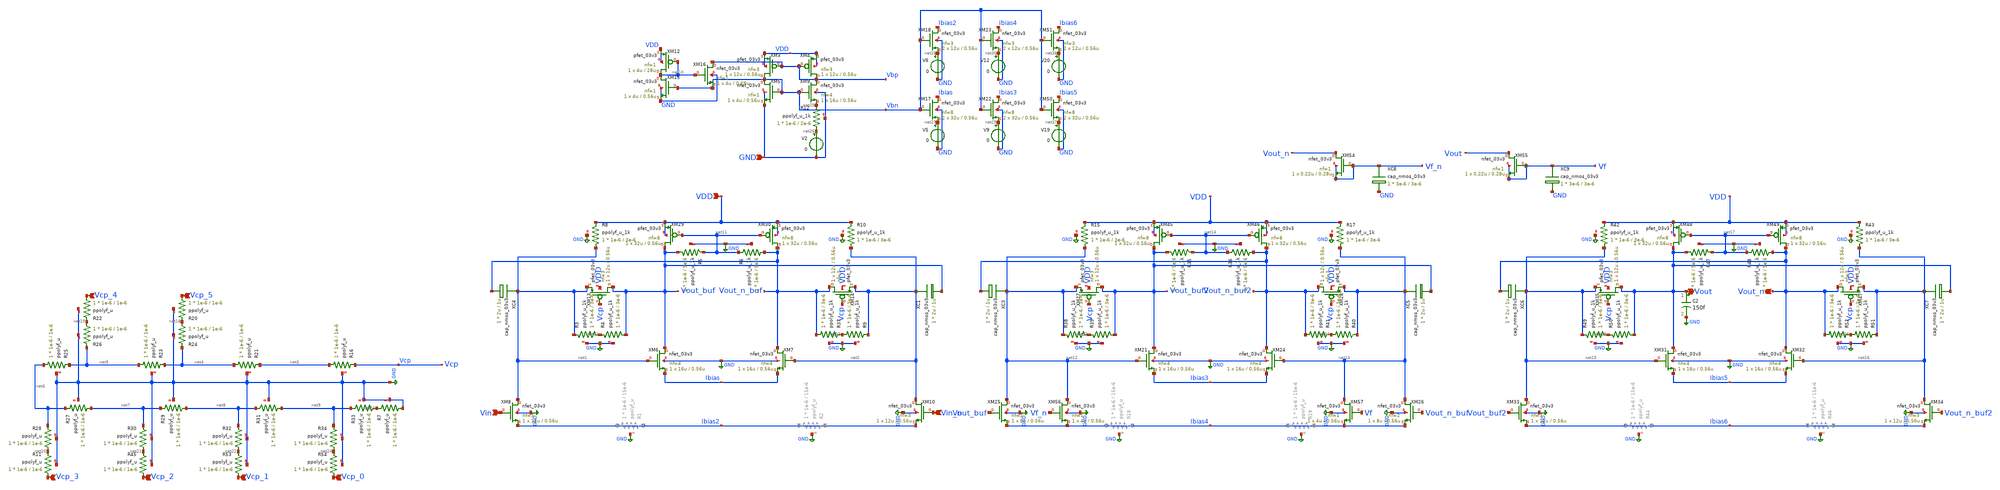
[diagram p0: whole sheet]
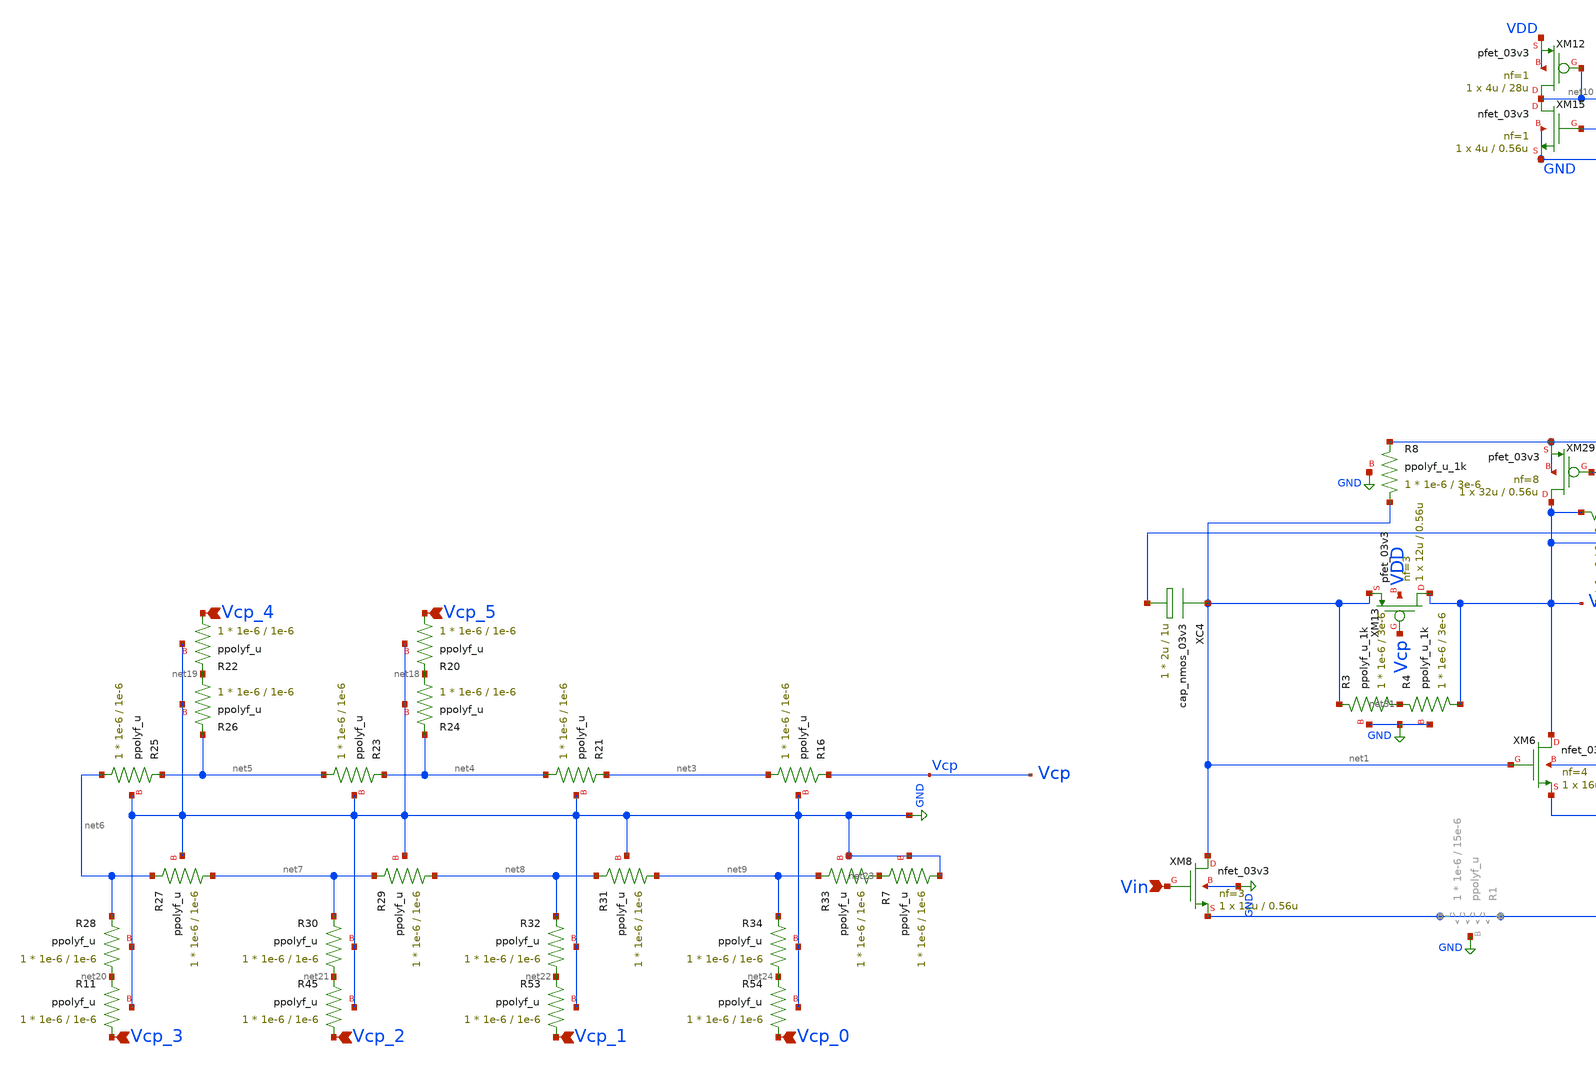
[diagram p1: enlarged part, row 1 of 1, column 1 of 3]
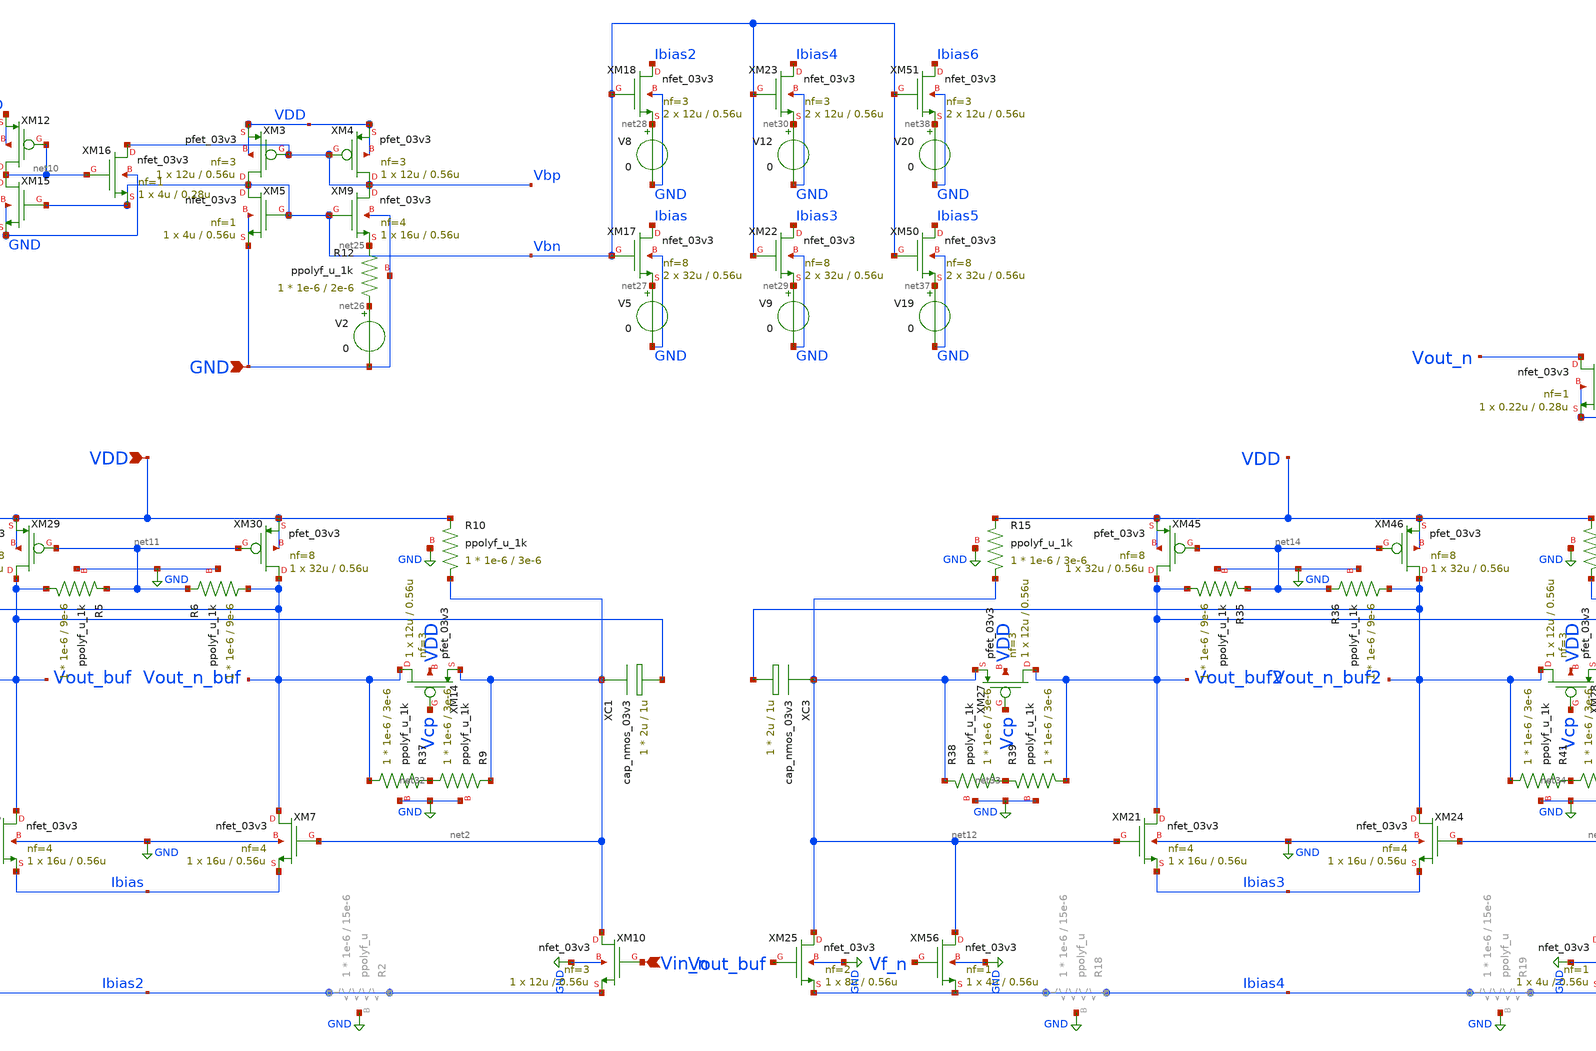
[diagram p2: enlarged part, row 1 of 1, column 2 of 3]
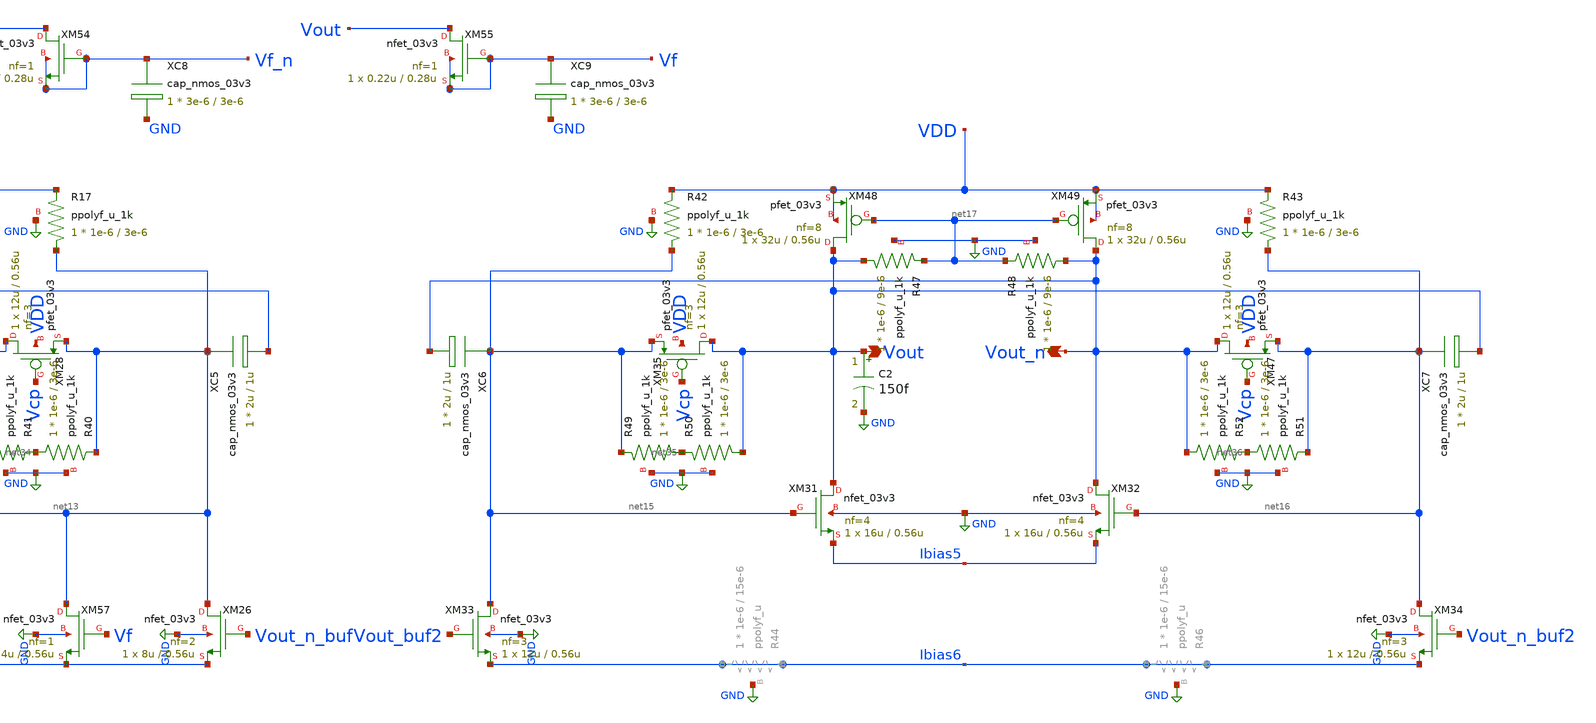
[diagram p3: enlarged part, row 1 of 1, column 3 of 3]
** sch_path: blocks/adc/vga/vga.sch
**.subckt vga Vcp_0 Vcp_1 Vcp_2 Vcp_3 Vcp_4 Vcp_5 VDD Vin Vin_n Vout GND Vout_n
*.ipin Vcp_0
*.ipin Vcp_1
*.ipin Vcp_2
*.ipin Vcp_3
*.ipin Vcp_4
*.ipin Vcp_5
*.ipin VDD
*.ipin Vin
*.ipin Vin_n
*.opin Vout
*.ipin GND
*.opin Vout_n
XM6 Vout_buf net1 Ibias GND nfet_03v3 L=0.56u W=16u nf=4 ad='int((nf+1)/2) * W/nf * 0.18u' as='int((nf+2)/2) * W/nf * 0.18u'
+ pd='2*int((nf+1)/2) * (W/nf + 0.18u)' ps='2*int((nf+2)/2) * (W/nf + 0.18u)' nrd='0.18u / W' nrs='0.18u / W'
+ sa=0 sb=0 sd=0 m=1
XM7 Vout_n_buf net2 Ibias GND nfet_03v3 L=0.56u W=16u nf=4 ad='int((nf+1)/2) * W/nf * 0.18u' as='int((nf+2)/2) * W/nf * 0.18u'
+ pd='2*int((nf+1)/2) * (W/nf + 0.18u)' ps='2*int((nf+2)/2) * (W/nf + 0.18u)' nrd='0.18u / W' nrs='0.18u / W'
+ sa=0 sb=0 sd=0 m=1
XM8 net1 Vin Ibias2 GND nfet_03v3 L=0.56u W=12u nf=3 ad='int((nf+1)/2) * W/nf * 0.18u' as='int((nf+2)/2) * W/nf * 0.18u'
+ pd='2*int((nf+1)/2) * (W/nf + 0.18u)' ps='2*int((nf+2)/2) * (W/nf + 0.18u)' nrd='0.18u / W' nrs='0.18u / W'
+ sa=0 sb=0 sd=0 m=1
XM10 net2 Vin_n Ibias2 GND nfet_03v3 L=0.56u W=12u nf=3 ad='int((nf+1)/2) * W/nf * 0.18u' as='int((nf+2)/2) * W/nf * 0.18u'
+ pd='2*int((nf+1)/2) * (W/nf + 0.18u)' ps='2*int((nf+2)/2) * (W/nf + 0.18u)' nrd='0.18u / W' nrs='0.18u / W'
+ sa=0 sb=0 sd=0 m=1
XR16 net3 Vcp GND ppolyf_u r_width=1e-6 r_length=1e-6 m=1
XR21 net4 net3 GND ppolyf_u r_width=1e-6 r_length=1e-6 m=1
XR23 net5 net4 GND ppolyf_u r_width=1e-6 r_length=1e-6 m=1
XR24 net18 net4 GND ppolyf_u r_width=1e-6 r_length=1e-6 m=1
XR25 net6 net5 GND ppolyf_u r_width=1e-6 r_length=1e-6 m=1
XR26 net19 net5 GND ppolyf_u r_width=1e-6 r_length=1e-6 m=1
XR27 net7 net6 GND ppolyf_u r_width=1e-6 r_length=1e-6 m=1
XR28 net20 net6 GND ppolyf_u r_width=1e-6 r_length=1e-6 m=1
XR29 net8 net7 GND ppolyf_u r_width=1e-6 r_length=1e-6 m=1
XR30 net21 net7 GND ppolyf_u r_width=1e-6 r_length=1e-6 m=1
XR31 net9 net8 GND ppolyf_u r_width=1e-6 r_length=1e-6 m=1
XR32 net22 net8 GND ppolyf_u r_width=1e-6 r_length=1e-6 m=1
XR33 net23 net9 GND ppolyf_u r_width=1e-6 r_length=1e-6 m=1
XR34 net24 net9 GND ppolyf_u r_width=1e-6 r_length=1e-6 m=1
XM13 Vout_buf Vcp net1 VDD pfet_03v3 L=0.56u W=12u nf=3 ad='int((nf+1)/2) * W/nf * 0.18u' as='int((nf+2)/2) * W/nf * 0.18u'
+ pd='2*int((nf+1)/2) * (W/nf + 0.18u)' ps='2*int((nf+2)/2) * (W/nf + 0.18u)' nrd='0.18u / W' nrs='0.18u / W'
+ sa=0 sb=0 sd=0 m=1
XM14 Vout_n_buf Vcp net2 VDD pfet_03v3 L=0.56u W=12u nf=3 ad='int((nf+1)/2) * W/nf * 0.18u' as='int((nf+2)/2) * W/nf * 0.18u'
+ pd='2*int((nf+1)/2) * (W/nf + 0.18u)' ps='2*int((nf+2)/2) * (W/nf + 0.18u)' nrd='0.18u / W' nrs='0.18u / W'
+ sa=0 sb=0 sd=0 m=1
XR8 net1 VDD GND ppolyf_u_1k r_width=1e-6 r_length=3e-6 m=1
XR10 net2 VDD GND ppolyf_u_1k r_width=1e-6 r_length=3e-6 m=1
XC4 net1 Vout_n_buf cap_nmos_03v3 c_width=2u c_length=1u m=1
XC1 net2 Vout_buf cap_nmos_03v3 c_width=2u c_length=1u m=1
XM3 Vbn Vbp VDD VDD pfet_03v3 L=0.56u W=12u nf=3 ad='int((nf+1)/2) * W/nf * 0.18u' as='int((nf+2)/2) * W/nf * 0.18u'
+ pd='2*int((nf+1)/2) * (W/nf + 0.18u)' ps='2*int((nf+2)/2) * (W/nf + 0.18u)' nrd='0.18u / W' nrs='0.18u / W'
+ sa=0 sb=0 sd=0 m=1
XM4 Vbp Vbp VDD VDD pfet_03v3 L=0.56u W=12u nf=3 ad='int((nf+1)/2) * W/nf * 0.18u' as='int((nf+2)/2) * W/nf * 0.18u'
+ pd='2*int((nf+1)/2) * (W/nf + 0.18u)' ps='2*int((nf+2)/2) * (W/nf + 0.18u)' nrd='0.18u / W' nrs='0.18u / W'
+ sa=0 sb=0 sd=0 m=1
XM5 Vbn Vbn GND GND nfet_03v3 L=0.56u W=4u nf=1 ad='int((nf+1)/2) * W/nf * 0.18u' as='int((nf+2)/2) * W/nf * 0.18u'
+ pd='2*int((nf+1)/2) * (W/nf + 0.18u)' ps='2*int((nf+2)/2) * (W/nf + 0.18u)' nrd='0.18u / W' nrs='0.18u / W'
+ sa=0 sb=0 sd=0 m=1
XM9 Vbp Vbn net25 GND nfet_03v3 L=0.56u W=16u nf=4 ad='int((nf+1)/2) * W/nf * 0.18u' as='int((nf+2)/2) * W/nf * 0.18u'
+ pd='2*int((nf+1)/2) * (W/nf + 0.18u)' ps='2*int((nf+2)/2) * (W/nf + 0.18u)' nrd='0.18u / W' nrs='0.18u / W'
+ sa=0 sb=0 sd=0 m=1
XM12 net10 net10 VDD VDD pfet_03v3 L=28u W=4u nf=1 ad='int((nf+1)/2) * W/nf * 0.18u' as='int((nf+2)/2) * W/nf * 0.18u'
+ pd='2*int((nf+1)/2) * (W/nf + 0.18u)' ps='2*int((nf+2)/2) * (W/nf + 0.18u)' nrd='0.18u / W' nrs='0.18u / W'
+ sa=0 sb=0 sd=0 m=1
XM15 net10 Vbn GND GND nfet_03v3 L=0.56u W=4u nf=1 ad='int((nf+1)/2) * W/nf * 0.18u' as='int((nf+2)/2) * W/nf * 0.18u'
+ pd='2*int((nf+1)/2) * (W/nf + 0.18u)' ps='2*int((nf+2)/2) * (W/nf + 0.18u)' nrd='0.18u / W' nrs='0.18u / W'
+ sa=0 sb=0 sd=0 m=1
XM16 Vbp net10 Vbn GND nfet_03v3 L=0.28u W=4u nf=1 ad='int((nf+1)/2) * W/nf * 0.18u' as='int((nf+2)/2) * W/nf * 0.18u'
+ pd='2*int((nf+1)/2) * (W/nf + 0.18u)' ps='2*int((nf+2)/2) * (W/nf + 0.18u)' nrd='0.18u / W' nrs='0.18u / W'
+ sa=0 sb=0 sd=0 m=1
XR12 net26 net25 GND ppolyf_u_1k r_width=1e-6 r_length=2e-6 m=1
V2 net26 GND 0
XM17 Ibias Vbn net27 GND nfet_03v3 L=0.56u W=32u nf=8 ad='int((nf+1)/2) * W/nf * 0.18u' as='int((nf+2)/2) * W/nf * 0.18u'
+ pd='2*int((nf+1)/2) * (W/nf + 0.18u)' ps='2*int((nf+2)/2) * (W/nf + 0.18u)' nrd='0.18u / W' nrs='0.18u / W'
+ sa=0 sb=0 sd=0 m=2
V5 net27 GND 0
XM18 Ibias2 Vbn net28 GND nfet_03v3 L=0.56u W=12u nf=3 ad='int((nf+1)/2) * W/nf * 0.18u' as='int((nf+2)/2) * W/nf * 0.18u'
+ pd='2*int((nf+1)/2) * (W/nf + 0.18u)' ps='2*int((nf+2)/2) * (W/nf + 0.18u)' nrd='0.18u / W' nrs='0.18u / W'
+ sa=0 sb=0 sd=0 m=2
V8 net28 GND 0
XM22 Ibias3 Vbn net29 GND nfet_03v3 L=0.56u W=32u nf=8 ad='int((nf+1)/2) * W/nf * 0.18u' as='int((nf+2)/2) * W/nf * 0.18u'
+ pd='2*int((nf+1)/2) * (W/nf + 0.18u)' ps='2*int((nf+2)/2) * (W/nf + 0.18u)' nrd='0.18u / W' nrs='0.18u / W'
+ sa=0 sb=0 sd=0 m=2
V9 net29 GND 0
XM23 Ibias4 Vbn net30 GND nfet_03v3 L=0.56u W=12u nf=3 ad='int((nf+1)/2) * W/nf * 0.18u' as='int((nf+2)/2) * W/nf * 0.18u'
+ pd='2*int((nf+1)/2) * (W/nf + 0.18u)' ps='2*int((nf+2)/2) * (W/nf + 0.18u)' nrd='0.18u / W' nrs='0.18u / W'
+ sa=0 sb=0 sd=0 m=2
V12 net30 GND 0
XM29 Vout_buf net11 VDD VDD pfet_03v3 L=0.56u W=32u nf=8 ad='int((nf+1)/2) * W/nf * 0.18u' as='int((nf+2)/2) * W/nf * 0.18u'
+ pd='2*int((nf+1)/2) * (W/nf + 0.18u)' ps='2*int((nf+2)/2) * (W/nf + 0.18u)' nrd='0.18u / W' nrs='0.18u / W'
+ sa=0 sb=0 sd=0 m=1
XM30 Vout_n_buf net11 VDD VDD pfet_03v3 L=0.56u W=32u nf=8 ad='int((nf+1)/2) * W/nf * 0.18u' as='int((nf+2)/2) * W/nf * 0.18u'
+ pd='2*int((nf+1)/2) * (W/nf + 0.18u)' ps='2*int((nf+2)/2) * (W/nf + 0.18u)' nrd='0.18u / W' nrs='0.18u / W'
+ sa=0 sb=0 sd=0 m=1
XR5 Vout_buf net11 GND ppolyf_u_1k r_width=1e-6 r_length=9e-6 m=1
XR6 Vout_n_buf net11 GND ppolyf_u_1k r_width=1e-6 r_length=9e-6 m=1
XR3 net31 net1 GND ppolyf_u_1k r_width=1e-6 r_length=3e-6 m=1
XR4 Vout_buf net31 GND ppolyf_u_1k r_width=1e-6 r_length=3e-6 m=1
XR9 net32 net2 GND ppolyf_u_1k r_width=1e-6 r_length=3e-6 m=1
XR37 Vout_n_buf net32 GND ppolyf_u_1k r_width=1e-6 r_length=3e-6 m=1
XM21 Vout_buf2 net12 Ibias3 GND nfet_03v3 L=0.56u W=16u nf=4 ad='int((nf+1)/2) * W/nf * 0.18u' as='int((nf+2)/2) * W/nf * 0.18u'
+ pd='2*int((nf+1)/2) * (W/nf + 0.18u)' ps='2*int((nf+2)/2) * (W/nf + 0.18u)' nrd='0.18u / W' nrs='0.18u / W'
+ sa=0 sb=0 sd=0 m=1
XM24 Vout_n_buf2 net13 Ibias3 GND nfet_03v3 L=0.56u W=16u nf=4 ad='int((nf+1)/2) * W/nf * 0.18u' as='int((nf+2)/2) * W/nf * 0.18u'
+ pd='2*int((nf+1)/2) * (W/nf + 0.18u)' ps='2*int((nf+2)/2) * (W/nf + 0.18u)' nrd='0.18u / W' nrs='0.18u / W'
+ sa=0 sb=0 sd=0 m=1
XM25 net12 Vout_buf Ibias4 GND nfet_03v3 L=0.56u W=8u nf=2 ad='int((nf+1)/2) * W/nf * 0.18u' as='int((nf+2)/2) * W/nf * 0.18u'
+ pd='2*int((nf+1)/2) * (W/nf + 0.18u)' ps='2*int((nf+2)/2) * (W/nf + 0.18u)' nrd='0.18u / W' nrs='0.18u / W'
+ sa=0 sb=0 sd=0 m=1
XM26 net13 Vout_n_buf Ibias4 GND nfet_03v3 L=0.56u W=8u nf=2 ad='int((nf+1)/2) * W/nf * 0.18u' as='int((nf+2)/2) * W/nf * 0.18u'
+ pd='2*int((nf+1)/2) * (W/nf + 0.18u)' ps='2*int((nf+2)/2) * (W/nf + 0.18u)' nrd='0.18u / W' nrs='0.18u / W'
+ sa=0 sb=0 sd=0 m=1
XM27 Vout_buf2 Vcp net12 VDD pfet_03v3 L=0.56u W=12u nf=3 ad='int((nf+1)/2) * W/nf * 0.18u' as='int((nf+2)/2) * W/nf * 0.18u'
+ pd='2*int((nf+1)/2) * (W/nf + 0.18u)' ps='2*int((nf+2)/2) * (W/nf + 0.18u)' nrd='0.18u / W' nrs='0.18u / W'
+ sa=0 sb=0 sd=0 m=1
XM28 Vout_n_buf2 Vcp net13 VDD pfet_03v3 L=0.56u W=12u nf=3 ad='int((nf+1)/2) * W/nf * 0.18u' as='int((nf+2)/2) * W/nf * 0.18u'
+ pd='2*int((nf+1)/2) * (W/nf + 0.18u)' ps='2*int((nf+2)/2) * (W/nf + 0.18u)' nrd='0.18u / W' nrs='0.18u / W'
+ sa=0 sb=0 sd=0 m=1
XR15 net12 VDD GND ppolyf_u_1k r_width=1e-6 r_length=3e-6 m=1
XR17 net13 VDD GND ppolyf_u_1k r_width=1e-6 r_length=3e-6 m=1
XC3 net12 Vout_n_buf2 cap_nmos_03v3 c_width=2u c_length=1u m=1
XC5 net13 Vout_buf2 cap_nmos_03v3 c_width=2u c_length=1u m=1
XM45 Vout_buf2 net14 VDD VDD pfet_03v3 L=0.56u W=32u nf=8 ad='int((nf+1)/2) * W/nf * 0.18u' as='int((nf+2)/2) * W/nf * 0.18u'
+ pd='2*int((nf+1)/2) * (W/nf + 0.18u)' ps='2*int((nf+2)/2) * (W/nf + 0.18u)' nrd='0.18u / W' nrs='0.18u / W'
+ sa=0 sb=0 sd=0 m=1
XM46 Vout_n_buf2 net14 VDD VDD pfet_03v3 L=0.56u W=32u nf=8 ad='int((nf+1)/2) * W/nf * 0.18u' as='int((nf+2)/2) * W/nf * 0.18u'
+ pd='2*int((nf+1)/2) * (W/nf + 0.18u)' ps='2*int((nf+2)/2) * (W/nf + 0.18u)' nrd='0.18u / W' nrs='0.18u / W'
+ sa=0 sb=0 sd=0 m=1
XR35 Vout_buf2 net14 GND ppolyf_u_1k r_width=1e-6 r_length=9e-6 m=1
XR36 Vout_n_buf2 net14 GND ppolyf_u_1k r_width=1e-6 r_length=9e-6 m=1
XR38 net33 net12 GND ppolyf_u_1k r_width=1e-6 r_length=3e-6 m=1
XR39 Vout_buf2 net33 GND ppolyf_u_1k r_width=1e-6 r_length=3e-6 m=1
XR40 net34 net13 GND ppolyf_u_1k r_width=1e-6 r_length=3e-6 m=1
XR41 Vout_n_buf2 net34 GND ppolyf_u_1k r_width=1e-6 r_length=3e-6 m=1
XM31 Vout net15 Ibias5 GND nfet_03v3 L=0.56u W=16u nf=4 ad='int((nf+1)/2) * W/nf * 0.18u' as='int((nf+2)/2) * W/nf * 0.18u'
+ pd='2*int((nf+1)/2) * (W/nf + 0.18u)' ps='2*int((nf+2)/2) * (W/nf + 0.18u)' nrd='0.18u / W' nrs='0.18u / W'
+ sa=0 sb=0 sd=0 m=1
XM32 Vout_n net16 Ibias5 GND nfet_03v3 L=0.56u W=16u nf=4 ad='int((nf+1)/2) * W/nf * 0.18u' as='int((nf+2)/2) * W/nf * 0.18u'
+ pd='2*int((nf+1)/2) * (W/nf + 0.18u)' ps='2*int((nf+2)/2) * (W/nf + 0.18u)' nrd='0.18u / W' nrs='0.18u / W'
+ sa=0 sb=0 sd=0 m=1
XM33 net15 Vout_buf2 Ibias6 GND nfet_03v3 L=0.56u W=12u nf=3 ad='int((nf+1)/2) * W/nf * 0.18u' as='int((nf+2)/2) * W/nf * 0.18u'
+ pd='2*int((nf+1)/2) * (W/nf + 0.18u)' ps='2*int((nf+2)/2) * (W/nf + 0.18u)' nrd='0.18u / W' nrs='0.18u / W'
+ sa=0 sb=0 sd=0 m=1
XM34 net16 Vout_n_buf2 Ibias6 GND nfet_03v3 L=0.56u W=12u nf=3 ad='int((nf+1)/2) * W/nf * 0.18u' as='int((nf+2)/2) * W/nf * 0.18u'
+ pd='2*int((nf+1)/2) * (W/nf + 0.18u)' ps='2*int((nf+2)/2) * (W/nf + 0.18u)' nrd='0.18u / W' nrs='0.18u / W'
+ sa=0 sb=0 sd=0 m=1
XM35 Vout Vcp net15 VDD pfet_03v3 L=0.56u W=12u nf=3 ad='int((nf+1)/2) * W/nf * 0.18u' as='int((nf+2)/2) * W/nf * 0.18u'
+ pd='2*int((nf+1)/2) * (W/nf + 0.18u)' ps='2*int((nf+2)/2) * (W/nf + 0.18u)' nrd='0.18u / W' nrs='0.18u / W'
+ sa=0 sb=0 sd=0 m=1
XM47 Vout_n Vcp net16 VDD pfet_03v3 L=0.56u W=12u nf=3 ad='int((nf+1)/2) * W/nf * 0.18u' as='int((nf+2)/2) * W/nf * 0.18u'
+ pd='2*int((nf+1)/2) * (W/nf + 0.18u)' ps='2*int((nf+2)/2) * (W/nf + 0.18u)' nrd='0.18u / W' nrs='0.18u / W'
+ sa=0 sb=0 sd=0 m=1
XR42 net15 VDD GND ppolyf_u_1k r_width=1e-6 r_length=3e-6 m=1
XR43 net16 VDD GND ppolyf_u_1k r_width=1e-6 r_length=3e-6 m=1
XC6 net15 Vout_n cap_nmos_03v3 c_width=2u c_length=1u m=1
XC7 net16 Vout cap_nmos_03v3 c_width=2u c_length=1u m=1
XM48 Vout net17 VDD VDD pfet_03v3 L=0.56u W=32u nf=8 ad='int((nf+1)/2) * W/nf * 0.18u' as='int((nf+2)/2) * W/nf * 0.18u'
+ pd='2*int((nf+1)/2) * (W/nf + 0.18u)' ps='2*int((nf+2)/2) * (W/nf + 0.18u)' nrd='0.18u / W' nrs='0.18u / W'
+ sa=0 sb=0 sd=0 m=1
XM49 Vout_n net17 VDD VDD pfet_03v3 L=0.56u W=32u nf=8 ad='int((nf+1)/2) * W/nf * 0.18u' as='int((nf+2)/2) * W/nf * 0.18u'
+ pd='2*int((nf+1)/2) * (W/nf + 0.18u)' ps='2*int((nf+2)/2) * (W/nf + 0.18u)' nrd='0.18u / W' nrs='0.18u / W'
+ sa=0 sb=0 sd=0 m=1
XR47 Vout net17 GND ppolyf_u_1k r_width=1e-6 r_length=9e-6 m=1
XR48 Vout_n net17 GND ppolyf_u_1k r_width=1e-6 r_length=9e-6 m=1
XR49 net35 net15 GND ppolyf_u_1k r_width=1e-6 r_length=3e-6 m=1
XR50 Vout net35 GND ppolyf_u_1k r_width=1e-6 r_length=3e-6 m=1
XR51 net36 net16 GND ppolyf_u_1k r_width=1e-6 r_length=3e-6 m=1
XR52 Vout_n net36 GND ppolyf_u_1k r_width=1e-6 r_length=3e-6 m=1
XM50 Ibias5 Vbn net37 GND nfet_03v3 L=0.56u W=32u nf=8 ad='int((nf+1)/2) * W/nf * 0.18u' as='int((nf+2)/2) * W/nf * 0.18u'
+ pd='2*int((nf+1)/2) * (W/nf + 0.18u)' ps='2*int((nf+2)/2) * (W/nf + 0.18u)' nrd='0.18u / W' nrs='0.18u / W'
+ sa=0 sb=0 sd=0 m=2
V19 net37 GND 0
XM51 Ibias6 Vbn net38 GND nfet_03v3 L=0.56u W=12u nf=3 ad='int((nf+1)/2) * W/nf * 0.18u' as='int((nf+2)/2) * W/nf * 0.18u'
+ pd='2*int((nf+1)/2) * (W/nf + 0.18u)' ps='2*int((nf+2)/2) * (W/nf + 0.18u)' nrd='0.18u / W' nrs='0.18u / W'
+ sa=0 sb=0 sd=0 m=2
V20 net38 GND 0
XM54 Vout_n Vf_n Vf_n Vf_n nfet_03v3 L=0.28u W=0.22u nf=1 ad='int((nf+1)/2) * W/nf * 0.18u' as='int((nf+2)/2) * W/nf * 0.18u'
+ pd='2*int((nf+1)/2) * (W/nf + 0.18u)' ps='2*int((nf+2)/2) * (W/nf + 0.18u)' nrd='0.18u / W' nrs='0.18u / W'
+ sa=0 sb=0 sd=0 m=1
XM55 Vout Vf Vf Vf nfet_03v3 L=0.28u W=0.22u nf=1 ad='int((nf+1)/2) * W/nf * 0.18u' as='int((nf+2)/2) * W/nf * 0.18u'
+ pd='2*int((nf+1)/2) * (W/nf + 0.18u)' ps='2*int((nf+2)/2) * (W/nf + 0.18u)' nrd='0.18u / W' nrs='0.18u / W'
+ sa=0 sb=0 sd=0 m=1
XM56 net12 Vf_n Ibias4 GND nfet_03v3 L=0.56u W=4u nf=1 ad='int((nf+1)/2) * W/nf * 0.18u' as='int((nf+2)/2) * W/nf * 0.18u'
+ pd='2*int((nf+1)/2) * (W/nf + 0.18u)' ps='2*int((nf+2)/2) * (W/nf + 0.18u)' nrd='0.18u / W' nrs='0.18u / W'
+ sa=0 sb=0 sd=0 m=1
XM57 net13 Vf Ibias4 GND nfet_03v3 L=0.56u W=4u nf=1 ad='int((nf+1)/2) * W/nf * 0.18u' as='int((nf+2)/2) * W/nf * 0.18u'
+ pd='2*int((nf+1)/2) * (W/nf + 0.18u)' ps='2*int((nf+2)/2) * (W/nf + 0.18u)' nrd='0.18u / W' nrs='0.18u / W'
+ sa=0 sb=0 sd=0 m=1
XC8 Vf_n GND cap_nmos_03v3 c_width=3e-6 c_length=3e-6 m=1
XC9 Vf GND cap_nmos_03v3 c_width=3e-6 c_length=3e-6 m=1
XR7 GND net23 GND ppolyf_u r_width=1e-6 r_length=1e-6 m=1
XR11 Vcp_3 net20 GND ppolyf_u r_width=1e-6 r_length=1e-6 m=1
XR45 Vcp_2 net21 GND ppolyf_u r_width=1e-6 r_length=1e-6 m=1
XR53 Vcp_1 net22 GND ppolyf_u r_width=1e-6 r_length=1e-6 m=1
XR54 Vcp_0 net24 GND ppolyf_u r_width=1e-6 r_length=1e-6 m=1
XR20 Vcp_5 net18 GND ppolyf_u r_width=1e-6 r_length=1e-6 m=1
XR22 Vcp_4 net19 GND ppolyf_u r_width=1e-6 r_length=1e-6 m=1
C2 Vout GND 150f m=1
**** begin user architecture code


.include /foss/pdks/gf180mcuD/libs.tech/ngspice/design.ngspice
.lib /foss/pdks/gf180mcuD/libs.tech/ngspice/sm141064.ngspice typical
.lib /foss/pdks/gf180mcuD/libs.tech/ngspice/sm141064.ngspice bjt_typical
.lib /foss/pdks/gf180mcuD/libs.tech/ngspice/sm141064.ngspice diode_typical
.lib /foss/pdks/gf180mcuD/libs.tech/ngspice/sm141064.ngspice res_typical
.lib /foss/pdks/gf180mcuD/libs.tech/ngspice/sm141064.ngspice mimcap_typical
.lib /foss/pdks/gf180mcuD/libs.tech/ngspice/sm141064.ngspice moscap_typical
.option method=gear

VDD_src VDD 0 DC 3.3
* GND_src GND 0 DC 0
Vin_src Vin 0 DC 1.65 AC 10m 0
Vin_n_src Vin_n 0 DC 1.65 AC 10m 180

VCP5_src Vcp_5 0 DC 3.3
VCP4_src Vcp_4 0 DC 3.3
VCP3_src Vcp_3 0 DC 3.3
VCP2_src Vcp_2 0 DC 3.3
VCP1_src Vcp_1 0 DC 3.3
VCP0_src Vcp_0 0 DC 3.3

.control
set temp = 25
  * 1. Setup the sweep parameters
  let v_ctrl = 3.3

  let f_start = 1
  let f_stop = 3.2G
  let f_points = 120

  * 2. Initialize vectors to store results
  let gain_db = unitvec(f_points)

  alter v3 = v_ctrl
  ac dec $&f_points $&f_start $&f_stop

  * 4. Calculate Differential Gain in dB
  * Formula: 20 * log10(|Vout_diff| / |Vin_diff|)
  let vin_mag = mag(v(vin) - v(vin_n))
  let vout_s_mag = mag(v(vout))
  let vout_buf_mag = mag(v(vout) - v(vout_n))
  let vout_s_gain = 20 * log10(vout_s_mag / vin_mag)
  let vout_buf_gain = 20 * log10(vout_buf_mag / vin_mag)

  * Credit to marcel hendrix
  * https://sourceforge.net/p/ngspice/discussion/133842/thread/2031ad61/
  meas ac peak  MAX  vout_s_mag FROM=$&f_start TO=$&f_stop
  let f3db = peak/sqrt(2)
  meas ac lo_3db WHEN vout_s_mag=f3db RISE=1
  meas ac hi_3db WHEN vout_s_mag=f3db FALL=1

  meas ac peak  MAX  vout_buf_mag FROM=$&f_start TO=$&f_stop
  let f3db = peak/sqrt(2)
  meas ac lo_3db WHEN vout_buf_mag=f3db RISE=1
  meas ac hi_3db WHEN vout_buf_mag=f3db FALL=1

  * 5. Save results to vectors
  plot vout_s_gain vout_buf_gain title 'Gain (dB) vs. Frequency from 1MHz to 3.2GHz, 0.6 vctrl' ylimit
+ -20 60
.endc


**** end user architecture code
**.ends
.GLOBAL GND
.end
